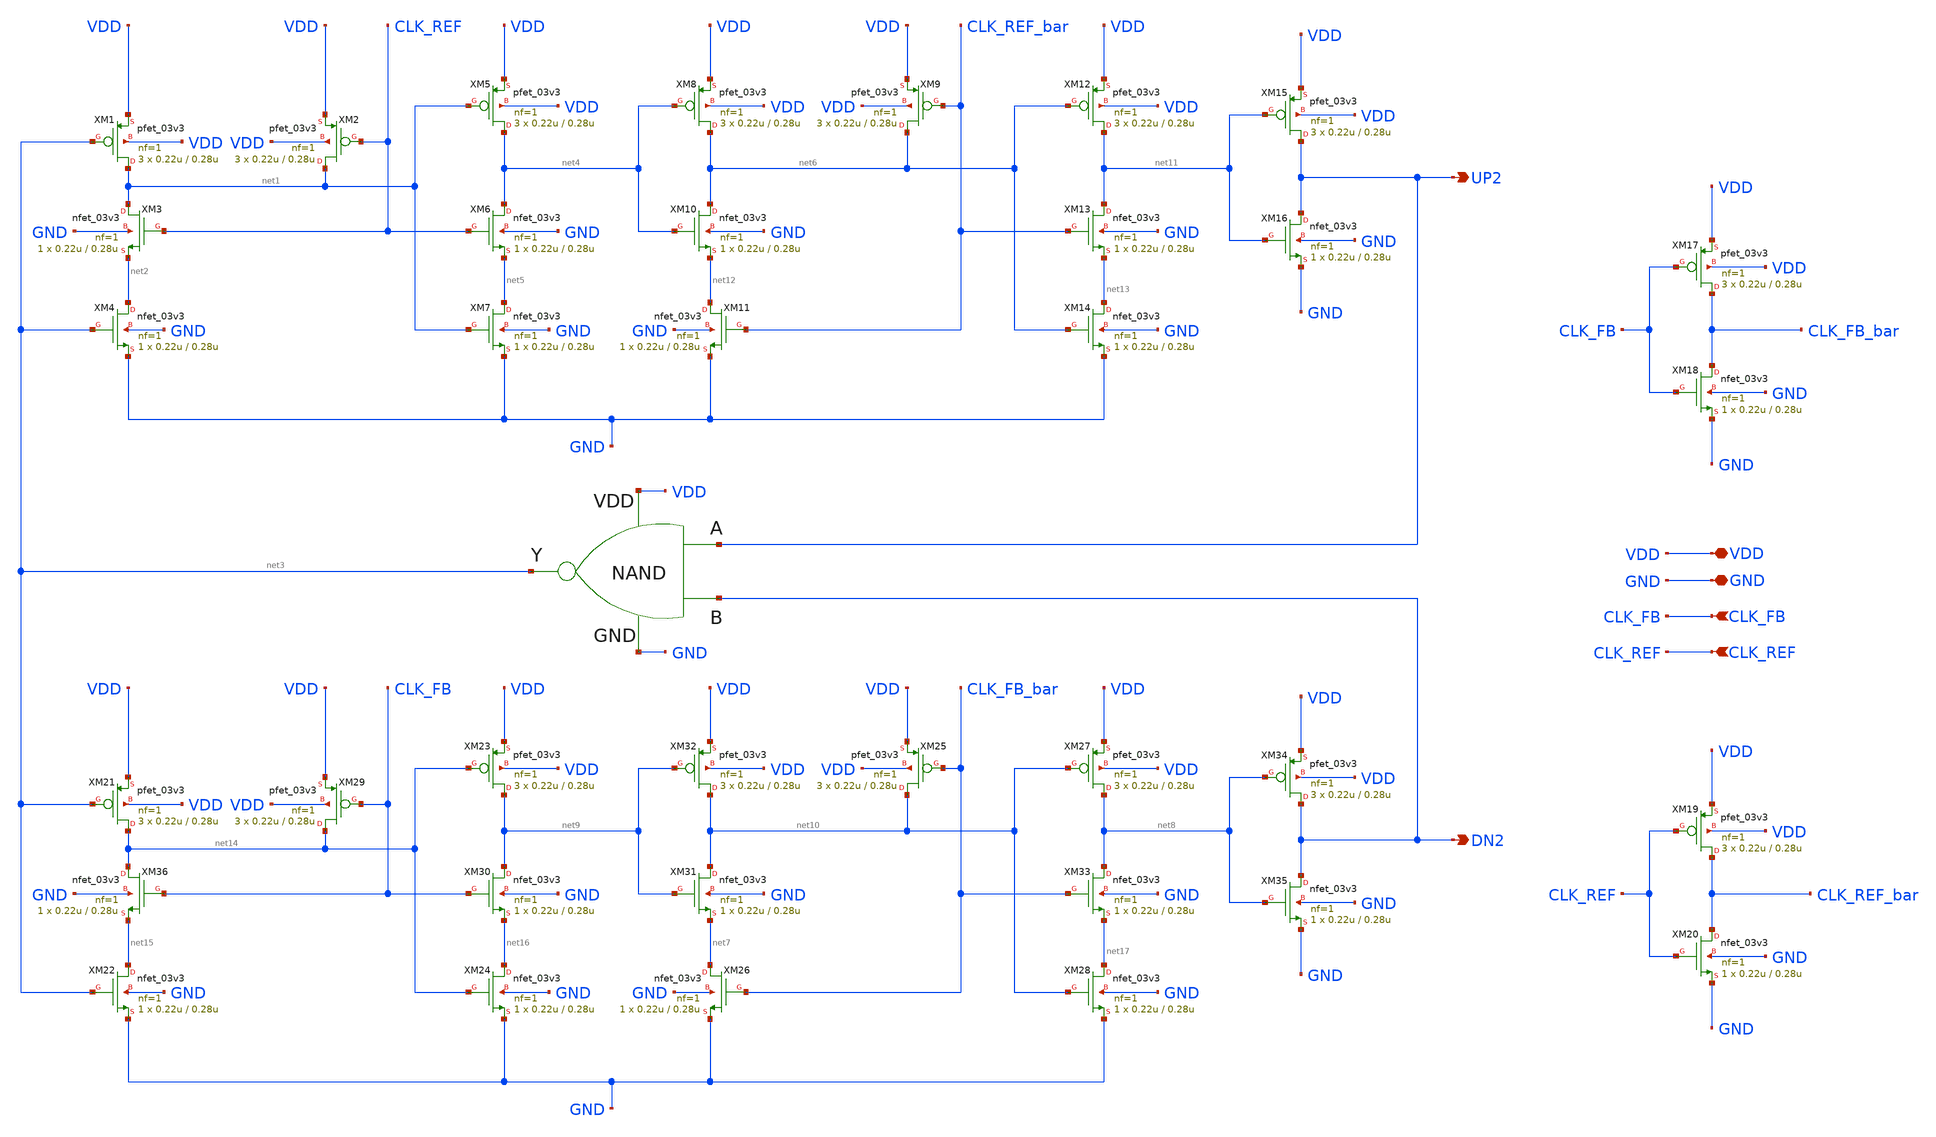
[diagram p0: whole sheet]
** sch_path: PFD/OPL_PFD.sch
**.subckt OPL_PFD UP2 CLK_FB CLK_REF DN2 VDD GND
*.opin UP2
*.ipin CLK_FB
*.ipin CLK_REF
*.opin DN2
*.iopin VDD
*.iopin GND
XM1 net1 net3 VDD VDD pfet_03v3 L=0.28u W=0.22u nf=1 ad='int((nf+1)/2) * W/nf * 0.18u' as='int((nf+2)/2) * W/nf * 0.18u'
+ pd='2*int((nf+1)/2) * (W/nf + 0.18u)' ps='2*int((nf+2)/2) * (W/nf + 0.18u)' nrd='0.18u / W' nrs='0.18u / W'
+ sa=0 sb=0 sd=0 m=3
XM4 net2 net3 GND GND nfet_03v3 L=0.28u W=0.22u nf=1 ad='int((nf+1)/2) * W/nf * 0.18u' as='int((nf+2)/2) * W/nf * 0.18u'
+ pd='2*int((nf+1)/2) * (W/nf + 0.18u)' ps='2*int((nf+2)/2) * (W/nf + 0.18u)' nrd='0.18u / W' nrs='0.18u / W'
+ sa=0 sb=0 sd=0 m=1
XM5 net4 net1 VDD VDD pfet_03v3 L=0.28u W=0.22u nf=1 ad='int((nf+1)/2) * W/nf * 0.18u' as='int((nf+2)/2) * W/nf * 0.18u'
+ pd='2*int((nf+1)/2) * (W/nf + 0.18u)' ps='2*int((nf+2)/2) * (W/nf + 0.18u)' nrd='0.18u / W' nrs='0.18u / W'
+ sa=0 sb=0 sd=0 m=3
XM7 net5 net1 GND GND nfet_03v3 L=0.28u W=0.22u nf=1 ad='int((nf+1)/2) * W/nf * 0.18u' as='int((nf+2)/2) * W/nf * 0.18u'
+ pd='2*int((nf+1)/2) * (W/nf + 0.18u)' ps='2*int((nf+2)/2) * (W/nf + 0.18u)' nrd='0.18u / W' nrs='0.18u / W'
+ sa=0 sb=0 sd=0 m=1
XM9 net6 CLK_REF_bar VDD VDD pfet_03v3 L=0.28u W=0.22u nf=1 ad='int((nf+1)/2) * W/nf * 0.18u' as='int((nf+2)/2) * W/nf * 0.18u'
+ pd='2*int((nf+1)/2) * (W/nf + 0.18u)' ps='2*int((nf+2)/2) * (W/nf + 0.18u)' nrd='0.18u / W' nrs='0.18u / W'
+ sa=0 sb=0 sd=0 m=3
XM11 net12 CLK_REF_bar GND GND nfet_03v3 L=0.28u W=0.22u nf=1 ad='int((nf+1)/2) * W/nf * 0.18u' as='int((nf+2)/2) * W/nf * 0.18u'
+ pd='2*int((nf+1)/2) * (W/nf + 0.18u)' ps='2*int((nf+2)/2) * (W/nf + 0.18u)' nrd='0.18u / W' nrs='0.18u / W'
+ sa=0 sb=0 sd=0 m=1
XM12 net11 net6 VDD VDD pfet_03v3 L=0.28u W=0.22u nf=1 ad='int((nf+1)/2) * W/nf * 0.18u' as='int((nf+2)/2) * W/nf * 0.18u'
+ pd='2*int((nf+1)/2) * (W/nf + 0.18u)' ps='2*int((nf+2)/2) * (W/nf + 0.18u)' nrd='0.18u / W' nrs='0.18u / W'
+ sa=0 sb=0 sd=0 m=3
XM14 net13 net6 GND GND nfet_03v3 L=0.28u W=0.22u nf=1 ad='int((nf+1)/2) * W/nf * 0.18u' as='int((nf+2)/2) * W/nf * 0.18u'
+ pd='2*int((nf+1)/2) * (W/nf + 0.18u)' ps='2*int((nf+2)/2) * (W/nf + 0.18u)' nrd='0.18u / W' nrs='0.18u / W'
+ sa=0 sb=0 sd=0 m=1
XM2 net1 CLK_REF VDD VDD pfet_03v3 L=0.28u W=0.22u nf=1 ad='int((nf+1)/2) * W/nf * 0.18u' as='int((nf+2)/2) * W/nf * 0.18u'
+ pd='2*int((nf+1)/2) * (W/nf + 0.18u)' ps='2*int((nf+2)/2) * (W/nf + 0.18u)' nrd='0.18u / W' nrs='0.18u / W'
+ sa=0 sb=0 sd=0 m=3
XM6 net4 CLK_REF net5 GND nfet_03v3 L=0.28u W=0.22u nf=1 ad='int((nf+1)/2) * W/nf * 0.18u' as='int((nf+2)/2) * W/nf * 0.18u'
+ pd='2*int((nf+1)/2) * (W/nf + 0.18u)' ps='2*int((nf+2)/2) * (W/nf + 0.18u)' nrd='0.18u / W' nrs='0.18u / W'
+ sa=0 sb=0 sd=0 m=1
XM10 net6 net4 net12 GND nfet_03v3 L=0.28u W=0.22u nf=1 ad='int((nf+1)/2) * W/nf * 0.18u' as='int((nf+2)/2) * W/nf * 0.18u'
+ pd='2*int((nf+1)/2) * (W/nf + 0.18u)' ps='2*int((nf+2)/2) * (W/nf + 0.18u)' nrd='0.18u / W' nrs='0.18u / W'
+ sa=0 sb=0 sd=0 m=1
XM8 net6 net4 VDD VDD pfet_03v3 L=0.28u W=0.22u nf=1 ad='int((nf+1)/2) * W/nf * 0.18u' as='int((nf+2)/2) * W/nf * 0.18u'
+ pd='2*int((nf+1)/2) * (W/nf + 0.18u)' ps='2*int((nf+2)/2) * (W/nf + 0.18u)' nrd='0.18u / W' nrs='0.18u / W'
+ sa=0 sb=0 sd=0 m=3
XM13 net11 CLK_REF_bar net13 GND nfet_03v3 L=0.28u W=0.22u nf=1 ad='int((nf+1)/2) * W/nf * 0.18u' as='int((nf+2)/2) * W/nf * 0.18u'
+ pd='2*int((nf+1)/2) * (W/nf + 0.18u)' ps='2*int((nf+2)/2) * (W/nf + 0.18u)' nrd='0.18u / W' nrs='0.18u / W'
+ sa=0 sb=0 sd=0 m=1
XM15 UP2 net11 VDD VDD pfet_03v3 L=0.28u W=0.22u nf=1 ad='int((nf+1)/2) * W/nf * 0.18u' as='int((nf+2)/2) * W/nf * 0.18u'
+ pd='2*int((nf+1)/2) * (W/nf + 0.18u)' ps='2*int((nf+2)/2) * (W/nf + 0.18u)' nrd='0.18u / W' nrs='0.18u / W'
+ sa=0 sb=0 sd=0 m=3
XM16 UP2 net11 GND GND nfet_03v3 L=0.28u W=0.22u nf=1 ad='int((nf+1)/2) * W/nf * 0.18u' as='int((nf+2)/2) * W/nf * 0.18u'
+ pd='2*int((nf+1)/2) * (W/nf + 0.18u)' ps='2*int((nf+2)/2) * (W/nf + 0.18u)' nrd='0.18u / W' nrs='0.18u / W'
+ sa=0 sb=0 sd=0 m=1
XM17 CLK_FB_bar CLK_FB VDD VDD pfet_03v3 L=0.28u W=0.22u nf=1 ad='int((nf+1)/2) * W/nf * 0.18u' as='int((nf+2)/2) * W/nf * 0.18u'
+ pd='2*int((nf+1)/2) * (W/nf + 0.18u)' ps='2*int((nf+2)/2) * (W/nf + 0.18u)' nrd='0.18u / W' nrs='0.18u / W'
+ sa=0 sb=0 sd=0 m=3
XM18 CLK_FB_bar CLK_FB GND GND nfet_03v3 L=0.28u W=0.22u nf=1 ad='int((nf+1)/2) * W/nf * 0.18u' as='int((nf+2)/2) * W/nf * 0.18u'
+ pd='2*int((nf+1)/2) * (W/nf + 0.18u)' ps='2*int((nf+2)/2) * (W/nf + 0.18u)' nrd='0.18u / W' nrs='0.18u / W'
+ sa=0 sb=0 sd=0 m=1
XM19 CLK_REF_bar CLK_REF VDD VDD pfet_03v3 L=0.28u W=0.22u nf=1 ad='int((nf+1)/2) * W/nf * 0.18u' as='int((nf+2)/2) * W/nf * 0.18u'
+ pd='2*int((nf+1)/2) * (W/nf + 0.18u)' ps='2*int((nf+2)/2) * (W/nf + 0.18u)' nrd='0.18u / W' nrs='0.18u / W'
+ sa=0 sb=0 sd=0 m=3
XM20 CLK_REF_bar CLK_REF GND GND nfet_03v3 L=0.28u W=0.22u nf=1 ad='int((nf+1)/2) * W/nf * 0.18u' as='int((nf+2)/2) * W/nf * 0.18u'
+ pd='2*int((nf+1)/2) * (W/nf + 0.18u)' ps='2*int((nf+2)/2) * (W/nf + 0.18u)' nrd='0.18u / W' nrs='0.18u / W'
+ sa=0 sb=0 sd=0 m=1
XM3 net1 CLK_REF net2 GND nfet_03v3 L=0.28u W=0.22u nf=1 ad='int((nf+1)/2) * W/nf * 0.18u' as='int((nf+2)/2) * W/nf * 0.18u'
+ pd='2*int((nf+1)/2) * (W/nf + 0.18u)' ps='2*int((nf+2)/2) * (W/nf + 0.18u)' nrd='0.18u / W' nrs='0.18u / W'
+ sa=0 sb=0 sd=0 m=1
XM21 net14 net3 VDD VDD pfet_03v3 L=0.28u W=0.22u nf=1 ad='int((nf+1)/2) * W/nf * 0.18u' as='int((nf+2)/2) * W/nf * 0.18u'
+ pd='2*int((nf+1)/2) * (W/nf + 0.18u)' ps='2*int((nf+2)/2) * (W/nf + 0.18u)' nrd='0.18u / W' nrs='0.18u / W'
+ sa=0 sb=0 sd=0 m=3
XM22 net15 net3 GND GND nfet_03v3 L=0.28u W=0.22u nf=1 ad='int((nf+1)/2) * W/nf * 0.18u' as='int((nf+2)/2) * W/nf * 0.18u'
+ pd='2*int((nf+1)/2) * (W/nf + 0.18u)' ps='2*int((nf+2)/2) * (W/nf + 0.18u)' nrd='0.18u / W' nrs='0.18u / W'
+ sa=0 sb=0 sd=0 m=1
XM23 net9 net14 VDD VDD pfet_03v3 L=0.28u W=0.22u nf=1 ad='int((nf+1)/2) * W/nf * 0.18u' as='int((nf+2)/2) * W/nf * 0.18u'
+ pd='2*int((nf+1)/2) * (W/nf + 0.18u)' ps='2*int((nf+2)/2) * (W/nf + 0.18u)' nrd='0.18u / W' nrs='0.18u / W'
+ sa=0 sb=0 sd=0 m=3
XM24 net16 net14 GND GND nfet_03v3 L=0.28u W=0.22u nf=1 ad='int((nf+1)/2) * W/nf * 0.18u' as='int((nf+2)/2) * W/nf * 0.18u'
+ pd='2*int((nf+1)/2) * (W/nf + 0.18u)' ps='2*int((nf+2)/2) * (W/nf + 0.18u)' nrd='0.18u / W' nrs='0.18u / W'
+ sa=0 sb=0 sd=0 m=1
XM25 net10 CLK_FB_bar VDD VDD pfet_03v3 L=0.28u W=0.22u nf=1 ad='int((nf+1)/2) * W/nf * 0.18u' as='int((nf+2)/2) * W/nf * 0.18u'
+ pd='2*int((nf+1)/2) * (W/nf + 0.18u)' ps='2*int((nf+2)/2) * (W/nf + 0.18u)' nrd='0.18u / W' nrs='0.18u / W'
+ sa=0 sb=0 sd=0 m=3
XM26 net7 CLK_FB_bar GND GND nfet_03v3 L=0.28u W=0.22u nf=1 ad='int((nf+1)/2) * W/nf * 0.18u' as='int((nf+2)/2) * W/nf * 0.18u'
+ pd='2*int((nf+1)/2) * (W/nf + 0.18u)' ps='2*int((nf+2)/2) * (W/nf + 0.18u)' nrd='0.18u / W' nrs='0.18u / W'
+ sa=0 sb=0 sd=0 m=1
XM27 net8 net10 VDD VDD pfet_03v3 L=0.28u W=0.22u nf=1 ad='int((nf+1)/2) * W/nf * 0.18u' as='int((nf+2)/2) * W/nf * 0.18u'
+ pd='2*int((nf+1)/2) * (W/nf + 0.18u)' ps='2*int((nf+2)/2) * (W/nf + 0.18u)' nrd='0.18u / W' nrs='0.18u / W'
+ sa=0 sb=0 sd=0 m=3
XM28 net17 net10 GND GND nfet_03v3 L=0.28u W=0.22u nf=1 ad='int((nf+1)/2) * W/nf * 0.18u' as='int((nf+2)/2) * W/nf * 0.18u'
+ pd='2*int((nf+1)/2) * (W/nf + 0.18u)' ps='2*int((nf+2)/2) * (W/nf + 0.18u)' nrd='0.18u / W' nrs='0.18u / W'
+ sa=0 sb=0 sd=0 m=1
XM29 net14 CLK_FB VDD VDD pfet_03v3 L=0.28u W=0.22u nf=1 ad='int((nf+1)/2) * W/nf * 0.18u' as='int((nf+2)/2) * W/nf * 0.18u'
+ pd='2*int((nf+1)/2) * (W/nf + 0.18u)' ps='2*int((nf+2)/2) * (W/nf + 0.18u)' nrd='0.18u / W' nrs='0.18u / W'
+ sa=0 sb=0 sd=0 m=3
XM30 net9 CLK_FB net16 GND nfet_03v3 L=0.28u W=0.22u nf=1 ad='int((nf+1)/2) * W/nf * 0.18u' as='int((nf+2)/2) * W/nf * 0.18u'
+ pd='2*int((nf+1)/2) * (W/nf + 0.18u)' ps='2*int((nf+2)/2) * (W/nf + 0.18u)' nrd='0.18u / W' nrs='0.18u / W'
+ sa=0 sb=0 sd=0 m=1
XM31 net10 net9 net7 GND nfet_03v3 L=0.28u W=0.22u nf=1 ad='int((nf+1)/2) * W/nf * 0.18u' as='int((nf+2)/2) * W/nf * 0.18u'
+ pd='2*int((nf+1)/2) * (W/nf + 0.18u)' ps='2*int((nf+2)/2) * (W/nf + 0.18u)' nrd='0.18u / W' nrs='0.18u / W'
+ sa=0 sb=0 sd=0 m=1
XM32 net10 net9 VDD VDD pfet_03v3 L=0.28u W=0.22u nf=1 ad='int((nf+1)/2) * W/nf * 0.18u' as='int((nf+2)/2) * W/nf * 0.18u'
+ pd='2*int((nf+1)/2) * (W/nf + 0.18u)' ps='2*int((nf+2)/2) * (W/nf + 0.18u)' nrd='0.18u / W' nrs='0.18u / W'
+ sa=0 sb=0 sd=0 m=3
XM33 net8 CLK_FB_bar net17 GND nfet_03v3 L=0.28u W=0.22u nf=1 ad='int((nf+1)/2) * W/nf * 0.18u' as='int((nf+2)/2) * W/nf * 0.18u'
+ pd='2*int((nf+1)/2) * (W/nf + 0.18u)' ps='2*int((nf+2)/2) * (W/nf + 0.18u)' nrd='0.18u / W' nrs='0.18u / W'
+ sa=0 sb=0 sd=0 m=1
XM34 DN2 net8 VDD VDD pfet_03v3 L=0.28u W=0.22u nf=1 ad='int((nf+1)/2) * W/nf * 0.18u' as='int((nf+2)/2) * W/nf * 0.18u'
+ pd='2*int((nf+1)/2) * (W/nf + 0.18u)' ps='2*int((nf+2)/2) * (W/nf + 0.18u)' nrd='0.18u / W' nrs='0.18u / W'
+ sa=0 sb=0 sd=0 m=3
XM35 DN2 net8 GND GND nfet_03v3 L=0.28u W=0.22u nf=1 ad='int((nf+1)/2) * W/nf * 0.18u' as='int((nf+2)/2) * W/nf * 0.18u'
+ pd='2*int((nf+1)/2) * (W/nf + 0.18u)' ps='2*int((nf+2)/2) * (W/nf + 0.18u)' nrd='0.18u / W' nrs='0.18u / W'
+ sa=0 sb=0 sd=0 m=1
XM36 net14 CLK_FB net15 GND nfet_03v3 L=0.28u W=0.22u nf=1 ad='int((nf+1)/2) * W/nf * 0.18u' as='int((nf+2)/2) * W/nf * 0.18u'
+ pd='2*int((nf+1)/2) * (W/nf + 0.18u)' ps='2*int((nf+2)/2) * (W/nf + 0.18u)' nrd='0.18u / W' nrs='0.18u / W'
+ sa=0 sb=0 sd=0 m=1
x1 GND UP2 DN2 VDD net3 NAND
**.ends

* expanding   symbol:  NAND.sym # of pins=5
** sym_path: PFD/NAND.sym
** sch_path: PFD/NAND.sch
.subckt NAND GND A B VDD Y
*.opin Y
*.ipin GND
*.ipin VDD
*.ipin A
*.ipin B
XM1 Y A VDD VDD pfet_03v3 L=0.28u W=0.22u nf=1 ad='int((nf+1)/2) * W/nf * 0.18u' as='int((nf+2)/2) * W/nf * 0.18u'
+ pd='2*int((nf+1)/2) * (W/nf + 0.18u)' ps='2*int((nf+2)/2) * (W/nf + 0.18u)' nrd='0.18u / W' nrs='0.18u / W'
+ sa=0 sb=0 sd=0 m=3
XM3 Y A net1 GND nfet_03v3 L=0.28u W=0.22u nf=1 ad='int((nf+1)/2) * W/nf * 0.18u' as='int((nf+2)/2) * W/nf * 0.18u'
+ pd='2*int((nf+1)/2) * (W/nf + 0.18u)' ps='2*int((nf+2)/2) * (W/nf + 0.18u)' nrd='0.18u / W' nrs='0.18u / W'
+ sa=0 sb=0 sd=0 m=1
XM4 net1 B GND GND nfet_03v3 L=0.28u W=0.22u nf=1 ad='int((nf+1)/2) * W/nf * 0.18u' as='int((nf+2)/2) * W/nf * 0.18u'
+ pd='2*int((nf+1)/2) * (W/nf + 0.18u)' ps='2*int((nf+2)/2) * (W/nf + 0.18u)' nrd='0.18u / W' nrs='0.18u / W'
+ sa=0 sb=0 sd=0 m=1
XM2 Y B VDD VDD pfet_03v3 L=0.28u W=0.22u nf=1 ad='int((nf+1)/2) * W/nf * 0.18u' as='int((nf+2)/2) * W/nf * 0.18u'
+ pd='2*int((nf+1)/2) * (W/nf + 0.18u)' ps='2*int((nf+2)/2) * (W/nf + 0.18u)' nrd='0.18u / W' nrs='0.18u / W'
+ sa=0 sb=0 sd=0 m=3
.ends

.end
